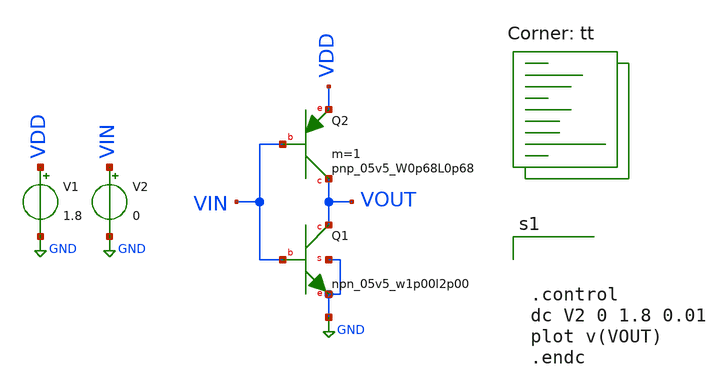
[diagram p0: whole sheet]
** sch_path: xsch/ip/bjt_test/inv_BJT.sch
**.subckt inv_BJT
V1 VDD GND 1.8
V2 VIN GND 0
XQ1 VOUT VIN GND GND sky130_fd_pr__npn_05v5_w1p00l2p00
XQ2 VOUT VIN VDD sky130_fd_pr__pnp_05v5_W0p68L0p68 m=1
**** begin user architecture code
.lib $::SKYWATER_MODELS/sky130.lib.spice tt



.control
dc V2 0 1.8 0.01
plot v(VOUT)
.endc



**** end user architecture code
**.ends
.GLOBAL GND
.end
